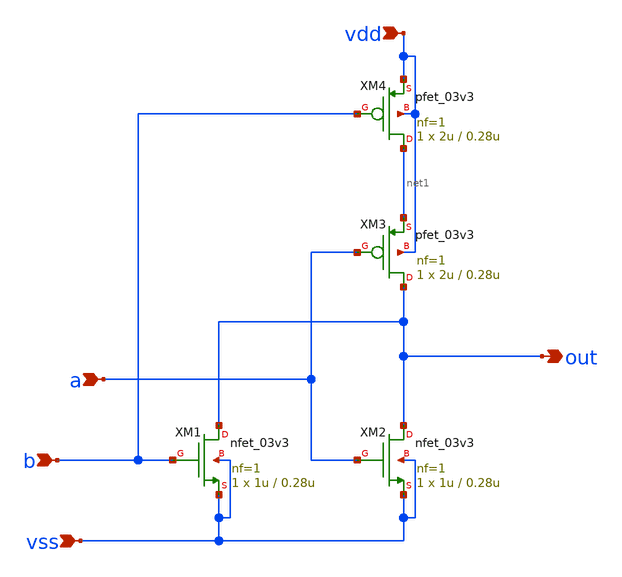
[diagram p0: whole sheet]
** sch_path: xschem/nor2.sch
**.subckt nor2 a b vss vdd out
*.ipin a
*.ipin b
*.ipin vss
*.ipin vdd
*.opin out
XM1 out b vss vss nfet_03v3 L=0.28u W=1u nf=1 ad='int((nf+1)/2) * W/nf * 0.18u' as='int((nf+2)/2) * W/nf * 0.18u'
+ pd='2*int((nf+1)/2) * (W/nf + 0.18u)' ps='2*int((nf+2)/2) * (W/nf + 0.18u)' nrd='0.18u / W' nrs='0.18u / W'
+ sa=0 sb=0 sd=0 m=1
XM2 out a vss vss nfet_03v3 L=0.28u W=1u nf=1 ad='int((nf+1)/2) * W/nf * 0.18u' as='int((nf+2)/2) * W/nf * 0.18u'
+ pd='2*int((nf+1)/2) * (W/nf + 0.18u)' ps='2*int((nf+2)/2) * (W/nf + 0.18u)' nrd='0.18u / W' nrs='0.18u / W'
+ sa=0 sb=0 sd=0 m=1
XM3 out a net1 vdd pfet_03v3 L=0.28u W=2u nf=1 ad='int((nf+1)/2) * W/nf * 0.18u' as='int((nf+2)/2) * W/nf * 0.18u'
+ pd='2*int((nf+1)/2) * (W/nf + 0.18u)' ps='2*int((nf+2)/2) * (W/nf + 0.18u)' nrd='0.18u / W' nrs='0.18u / W'
+ sa=0 sb=0 sd=0 m=1
XM4 net1 b vdd vdd pfet_03v3 L=0.28u W=2u nf=1 ad='int((nf+1)/2) * W/nf * 0.18u' as='int((nf+2)/2) * W/nf * 0.18u'
+ pd='2*int((nf+1)/2) * (W/nf + 0.18u)' ps='2*int((nf+2)/2) * (W/nf + 0.18u)' nrd='0.18u / W' nrs='0.18u / W'
+ sa=0 sb=0 sd=0 m=1
**.ends
.end
